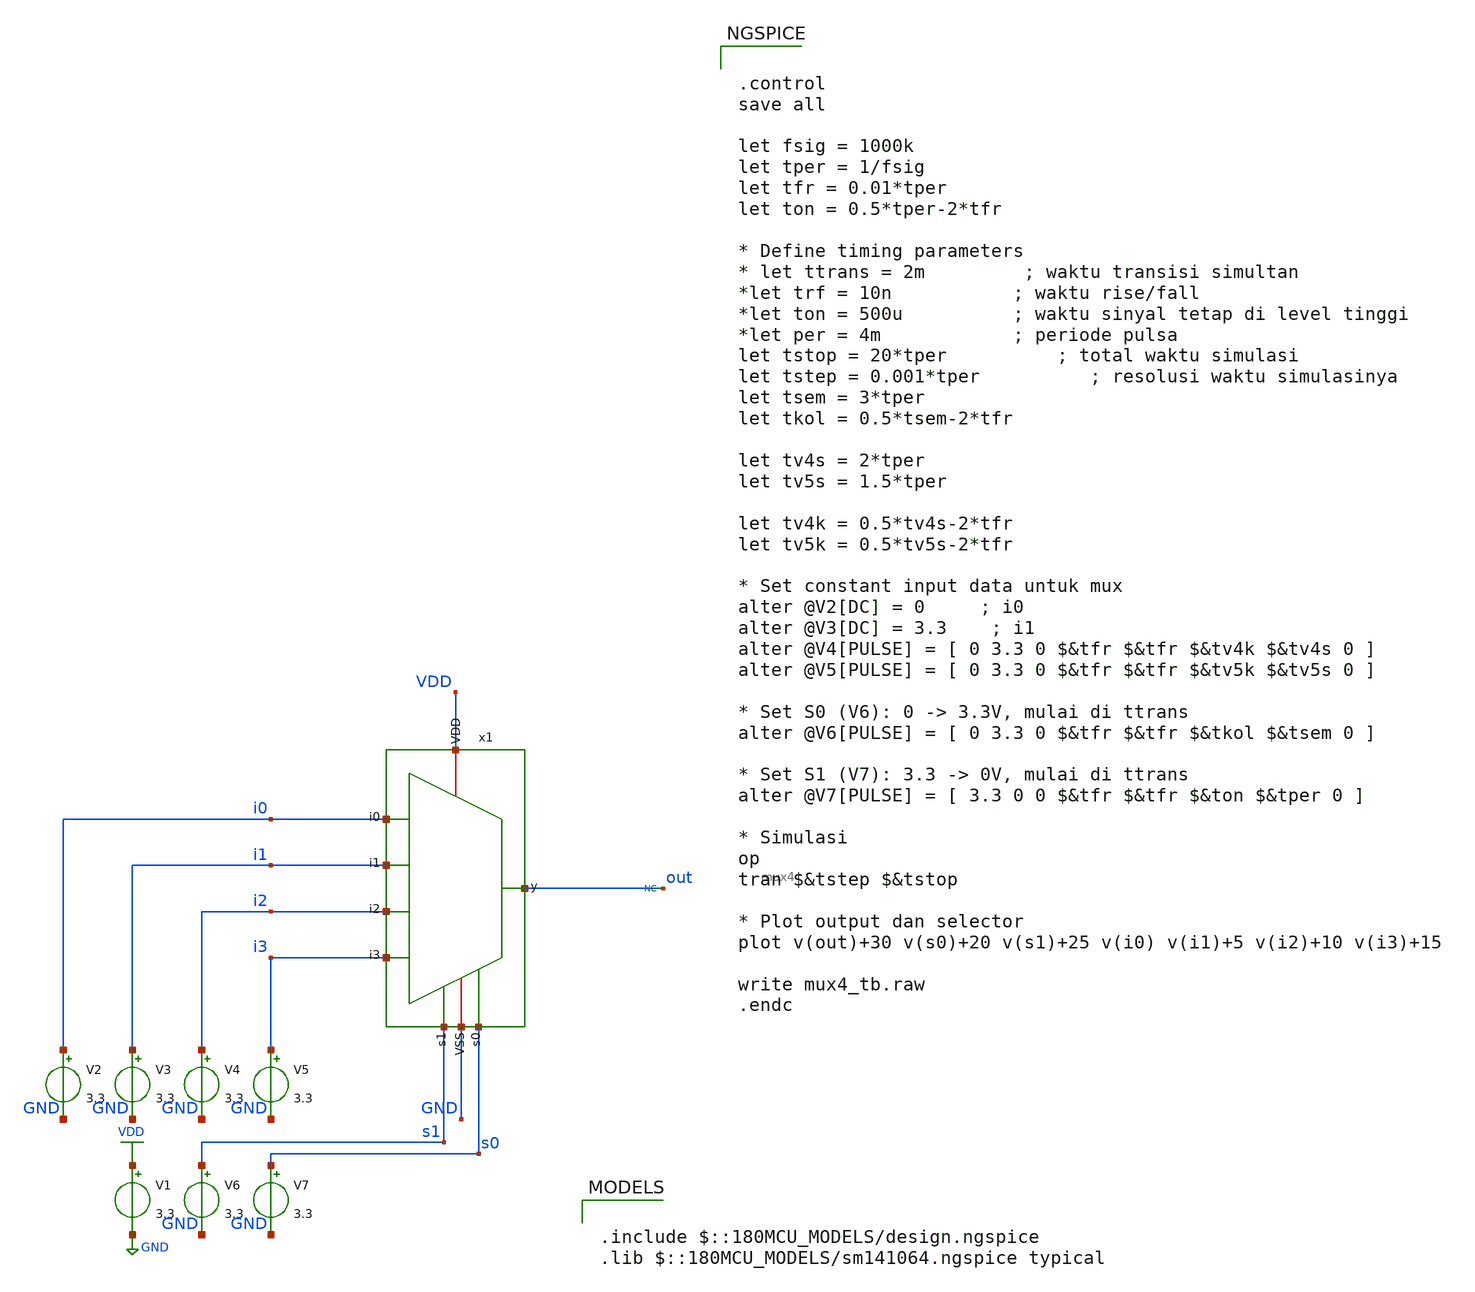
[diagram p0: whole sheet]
** sch_path: designs/test_4mux/mux4_tb.sch
**.subckt mux4_tb
V1 VDD GND 3.3
V2 i0 GND 3.3
V3 i1 GND 3.3
V4 i2 GND 3.3
V5 i3 GND 3.3
V6 s1 GND 3.3
V7 s0 GND 3.3
x1 GND i0 VDD s0 i1 out i2 s1 i3 mux4
* noconn out
**** begin user architecture code

.include $::180MCU_MODELS/design.ngspice
.lib $::180MCU_MODELS/sm141064.ngspice typical



.control
save all

let fsig = 1000k
let tper = 1/fsig
let tfr = 0.01*tper
let ton = 0.5*tper-2*tfr

* Define timing parameters
* let ttrans = 2m         ; waktu transisi simultan
*let trf = 10n           ; waktu rise/fall
*let ton = 500u          ; waktu sinyal tetap di level tinggi
*let per = 4m            ; periode pulsa
let tstop = 20*tper          ; total waktu simulasi
let tstep = 0.001*tper          ; resolusi waktu simulasinya
let tsem = 3*tper
let tkol = 0.5*tsem-2*tfr

let tv4s = 2*tper
let tv5s = 1.5*tper

let tv4k = 0.5*tv4s-2*tfr
let tv5k = 0.5*tv5s-2*tfr

* Set constant input data untuk mux
alter @V2[DC] = 0     ; i0
alter @V3[DC] = 3.3    ; i1
alter @V4[PULSE] = [ 0 3.3 0 $&tfr $&tfr $&tv4k $&tv4s 0 ]
alter @V5[PULSE] = [ 0 3.3 0 $&tfr $&tfr $&tv5k $&tv5s 0 ]

* Set S0 (V6): 0 -> 3.3V, mulai di ttrans
alter @V6[PULSE] = [ 0 3.3 0 $&tfr $&tfr $&tkol $&tsem 0 ]

* Set S1 (V7): 3.3 -> 0V, mulai di ttrans
alter @V7[PULSE] = [ 3.3 0 0 $&tfr $&tfr $&ton $&tper 0 ]

* Simulasi
op
tran $&tstep $&tstop

* Plot output dan selector
plot v(out)+30 v(s0)+20 v(s1)+25 v(i0) v(i1)+5 v(i2)+10 v(i3)+15

write mux4_tb.raw
.endc


**** end user architecture code
**.ends
.GLOBAL VDD
.GLOBAL GND
.end
